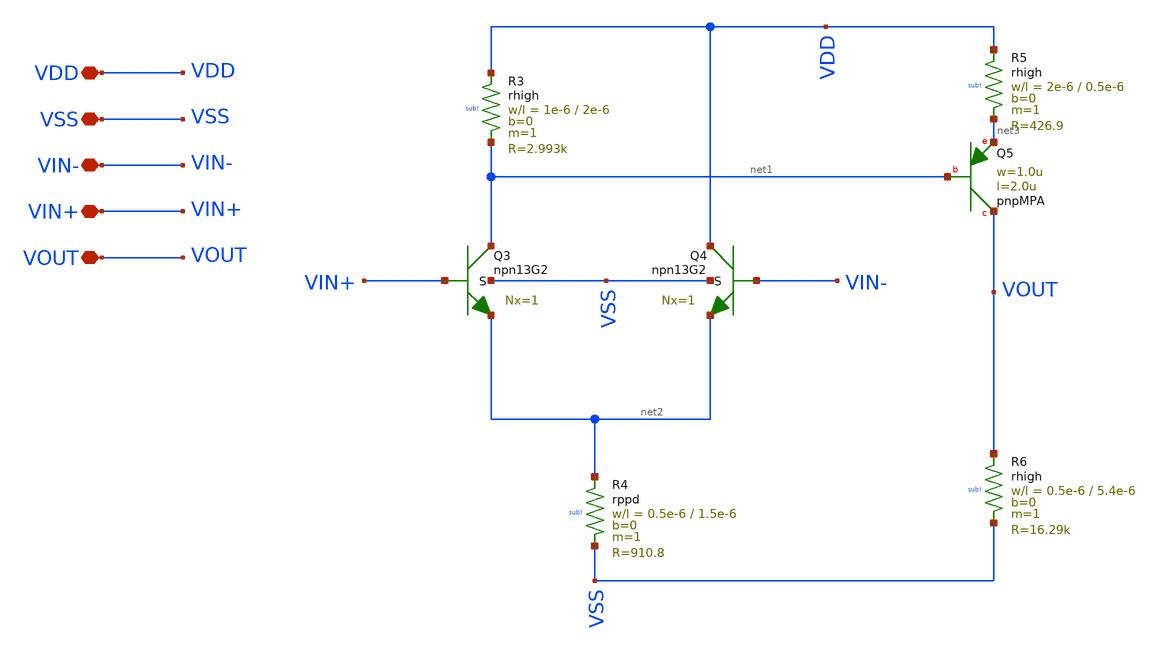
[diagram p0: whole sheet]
** sch_path: my_ip/LIB/ihp-sg13g2/Amplifiers/amp001_3_3_ihp-sg13g2.sch
**.subckt amp001_3_3_ihp-sg13g2 VDD VSS VIN- VIN+ VOUT
*.iopin VDD
*.iopin VSS
*.iopin VIN-
*.iopin VIN+
*.iopin VOUT
XQ3 net1 VIN+ net2 VSS npn13G2 Nx=1 mm_ok=1
XR3 VDD net1 sub! rhigh w=1e-6 l=2e-6 m=1 b=0 mm_ok=1
XR4 net2 VSS sub! rppd w=0.5e-6 l=1.5e-6 m=1 b=0 mm_ok=1
XQ4 VDD VIN- net2 VSS npn13G2 Nx=1 mm_ok=1
XQ5 VOUT net1 net3 pnpMPA a=2p p=6u m=1
XR5 VDD net3 sub! rhigh w=2e-6 l=0.5e-6 m=1 b=0 mm_ok=1
XR6 VOUT VSS sub! rhigh w=0.5e-6 l=5.4e-6 m=1 b=0 mm_ok=1
**** begin user architecture code
type=subcircuit
format="@name @pinlist @symname"
template="name=x1"
**** end user architecture code
**.ends
.end
